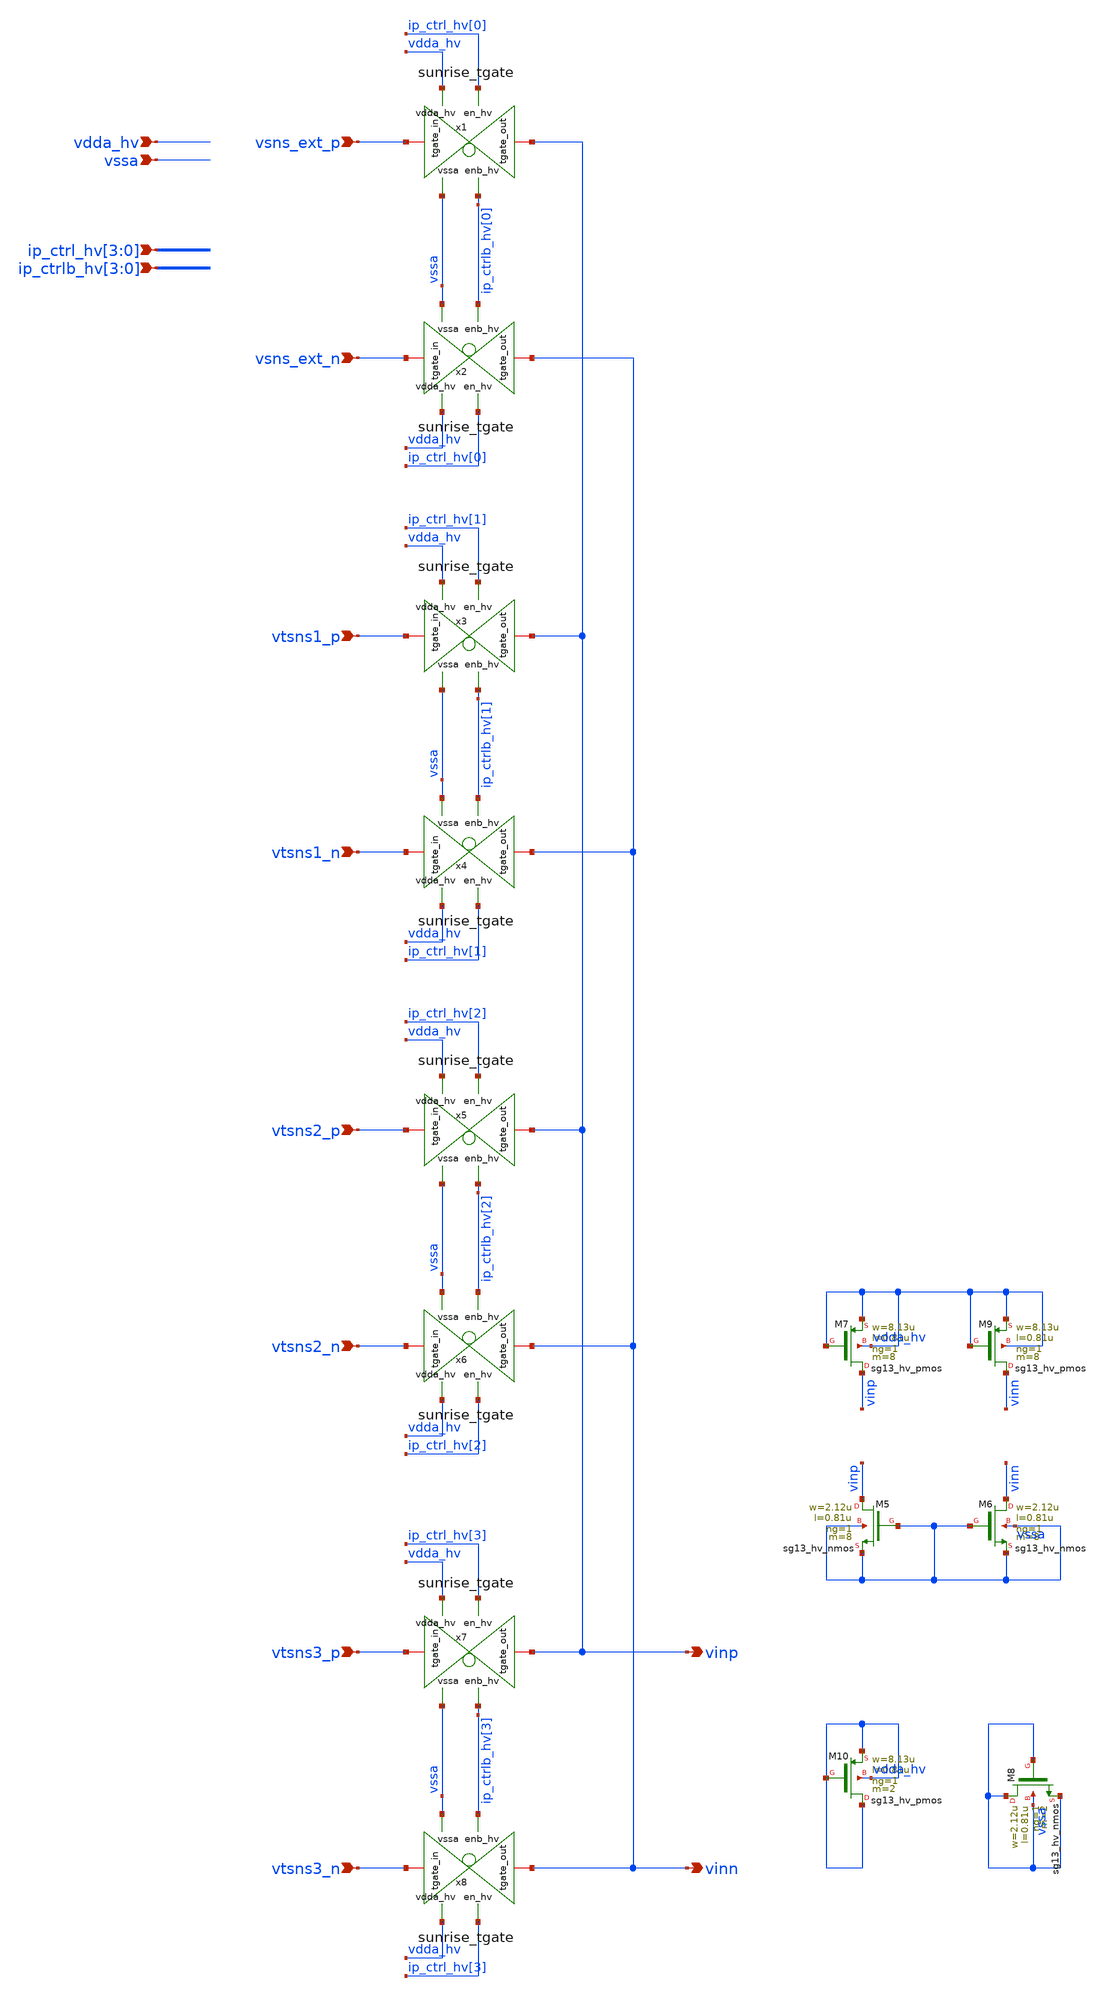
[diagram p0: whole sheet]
** sch_path: Schematics_Layout/sunrise_mux/sunrise_mux.sch
**.subckt sunrise_mux ip_ctrl_hv[3],ip_ctrl_hv[2],ip_ctrl_hv[1],ip_ctrl_hv[0]
*+ ip_ctrlb_hv[3],ip_ctrlb_hv[2],ip_ctrlb_hv[1],ip_ctrlb_hv[0] vdda_hv vssa vinp vinn vsns_ext_p vsns_ext_n vtsns1_p vtsns1_n vtsns2_p vtsns2_n vtsns3_p vtsns3_n
*.ipin ip_ctrl_hv[3],ip_ctrl_hv[2],ip_ctrl_hv[1],ip_ctrl_hv[0]
*.ipin ip_ctrlb_hv[3],ip_ctrlb_hv[2],ip_ctrlb_hv[1],ip_ctrlb_hv[0]
*.ipin vdda_hv
*.ipin vssa
*.opin vinp
*.opin vinn
*.ipin vsns_ext_p
*.ipin vsns_ext_n
*.ipin vtsns1_p
*.ipin vtsns1_n
*.ipin vtsns2_p
*.ipin vtsns2_n
*.ipin vtsns3_p
*.ipin vtsns3_n
x1 vdda_hv vssa ip_ctrl_hv[0] vsns_ext_p vinp ip_ctrlb_hv[0] sunrise_tgate
x2 vdda_hv vssa ip_ctrl_hv[0] vsns_ext_n vinn ip_ctrlb_hv[0] sunrise_tgate
x3 vdda_hv vssa ip_ctrl_hv[1] vtsns1_p vinp ip_ctrlb_hv[1] sunrise_tgate
x4 vdda_hv vssa ip_ctrl_hv[1] vtsns1_n vinn ip_ctrlb_hv[1] sunrise_tgate
x5 vdda_hv vssa ip_ctrl_hv[2] vtsns2_p vinp ip_ctrlb_hv[2] sunrise_tgate
x6 vdda_hv vssa ip_ctrl_hv[2] vtsns2_n vinn ip_ctrlb_hv[2] sunrise_tgate
x7 vdda_hv vssa ip_ctrl_hv[3] vtsns3_p vinp ip_ctrlb_hv[3] sunrise_tgate
x8 vdda_hv vssa ip_ctrl_hv[3] vtsns3_n vinn ip_ctrlb_hv[3] sunrise_tgate
XM5 vinp vssa vssa vssa sg13_hv_nmos w=2.12u l=0.81u ng=1 m=8 mm_ok=1
XM6 vinn vssa vssa vssa sg13_hv_nmos w=2.12u l=0.81u ng=1 m=8 mm_ok=1
XM7 vinp vdda_hv vdda_hv vdda_hv sg13_hv_pmos w=8.13u l=0.81u ng=1 m=8 mm_ok=1
XM9 vinn vdda_hv vdda_hv vdda_hv sg13_hv_pmos w=8.13u l=0.81u ng=1 m=8 mm_ok=1
XM8 vssa vssa vssa vssa sg13_hv_nmos w=2.12u l=0.81u ng=1 m=2 mm_ok=1
XM10 vdda_hv vdda_hv vdda_hv vdda_hv sg13_hv_pmos w=8.13u l=0.81u ng=1 m=2 mm_ok=1
**.ends
.end
